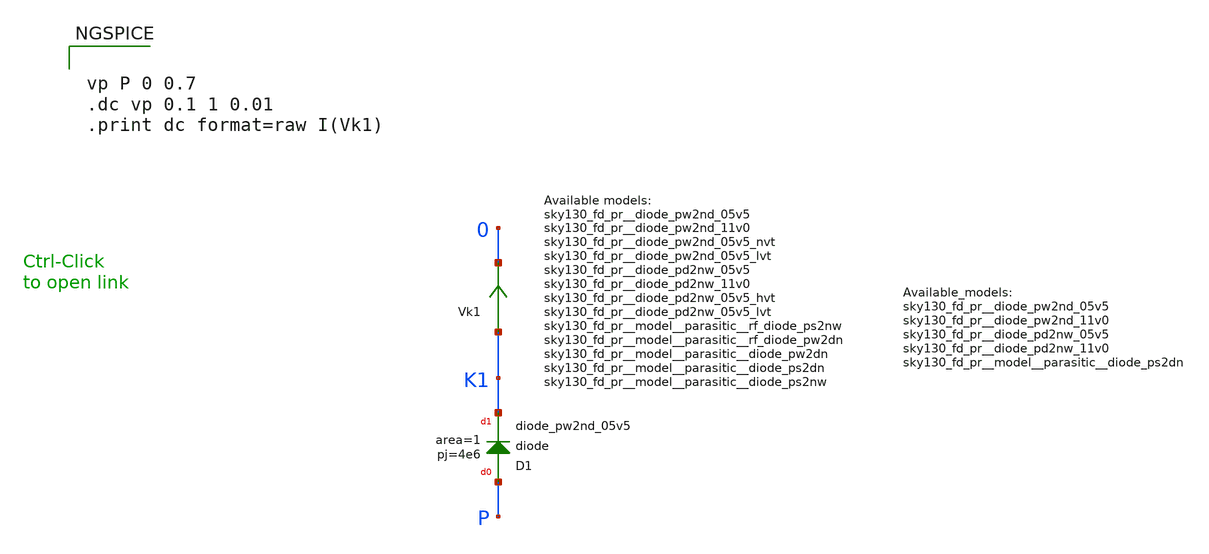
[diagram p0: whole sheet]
** sch_path: sky130_tests_X/test_diode2x.sch
* Copyright 2020 Stefan Frederik Schippers
* Licensed under the Apache License, Version 2.0 (the "License");
* you may not use this file except in compliance with the License.
* You may obtain a copy of the License at
* https://www.apache.org/licenses/LICENSE-2.0
* Unless required by applicable law or agreed to in writing, software
* distributed under the License is distributed on an "AS IS" BASIS,
* WITHOUT WARRANTIES OR CONDITIONS OF ANY KIND, either express or implied.
* See the License for the specific language governing permissions and
* limitations under the License.
**.subckt test_diode2x
Vk1 K1 0 0
.save i(vk1)
XD1 P K1 sky130_fd_pr__diode_pw2nd_05v5 area=1 pj=4e6
**** begin user architecture code


vp P 0 0.7
.dc vp 0.1 1 0.01
.print dc format=raw I(Vk1)



**** end user architecture code
**.ends
.end
